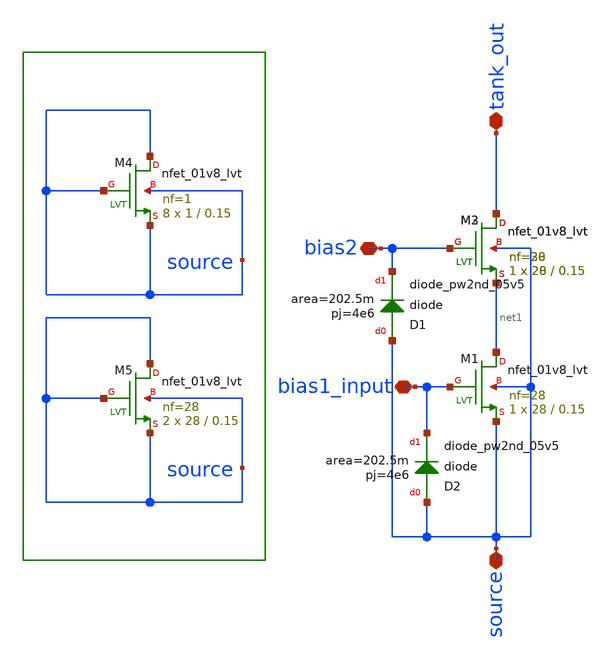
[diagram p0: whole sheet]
** sch_path: LNA_Vband/xschem/LNA_core/core_V3.1.sch
**.subckt core_V3.1 tank_out bias2 bias1_input source
*.iopin tank_out
*.iopin bias2
*.iopin bias1_input
*.iopin source
XM1 net1 bias1_input source source sky130_fd_pr__nfet_01v8_lvt L=0.15 W=28 nf=28 ad='int((nf+1)/2) * W/nf * 0.29'
+ as='int((nf+2)/2) * W/nf * 0.29' pd='2*int((nf+1)/2) * (W/nf + 0.29)' ps='2*int((nf+2)/2) * (W/nf + 0.29)'
+ nrd='0.29 / W' nrs='0.29 / W' sa=0 sb=0 sd=0 mult=1 m=1
XM2 tank_out bias2 net1 source sky130_fd_pr__nfet_01v8_lvt L=0.15 W=28 nf=28 ad='int((nf+1)/2) * W/nf * 0.29'
+ as='int((nf+2)/2) * W/nf * 0.29' pd='2*int((nf+1)/2) * (W/nf + 0.29)' ps='2*int((nf+2)/2) * (W/nf + 0.29)'
+ nrd='0.29 / W' nrs='0.29 / W' sa=0 sb=0 sd=0 mult=1 m=1
XM3 tank_out bias2 net1 source sky130_fd_pr__nfet_01v8_lvt L=0.15 W=20 nf=30 ad='int((nf+1)/2) * W/nf * 0.29'
+ as='int((nf+2)/2) * W/nf * 0.29' pd='2*int((nf+1)/2) * (W/nf + 0.29)' ps='2*int((nf+2)/2) * (W/nf + 0.29)'
+ nrd='0.29 / W' nrs='0.29 / W' sa=0 sb=0 sd=0 mult=1 m=1
XM4 source source source source sky130_fd_pr__nfet_01v8_lvt L=0.15 W=1 nf=1 ad='int((nf+1)/2) * W/nf * 0.29'
+ as='int((nf+2)/2) * W/nf * 0.29' pd='2*int((nf+1)/2) * (W/nf + 0.29)' ps='2*int((nf+2)/2) * (W/nf + 0.29)'
+ nrd='0.29 / W' nrs='0.29 / W' sa=0 sb=0 sd=0 mult=8 m=8
XM5 source source source source sky130_fd_pr__nfet_01v8_lvt L=0.15 W=28 nf=28 ad='int((nf+1)/2) * W/nf * 0.29'
+ as='int((nf+2)/2) * W/nf * 0.29' pd='2*int((nf+1)/2) * (W/nf + 0.29)' ps='2*int((nf+2)/2) * (W/nf + 0.29)'
+ nrd='0.29 / W' nrs='0.29 / W' sa=0 sb=0 sd=0 mult=2 m=2
XD2 source bias1_input sky130_fd_pr__diode_pw2nd_05v5 area=202.5m pj=4e6
XD1 source bias2 sky130_fd_pr__diode_pw2nd_05v5 area=202.5m pj=4e6
**.ends
.end
